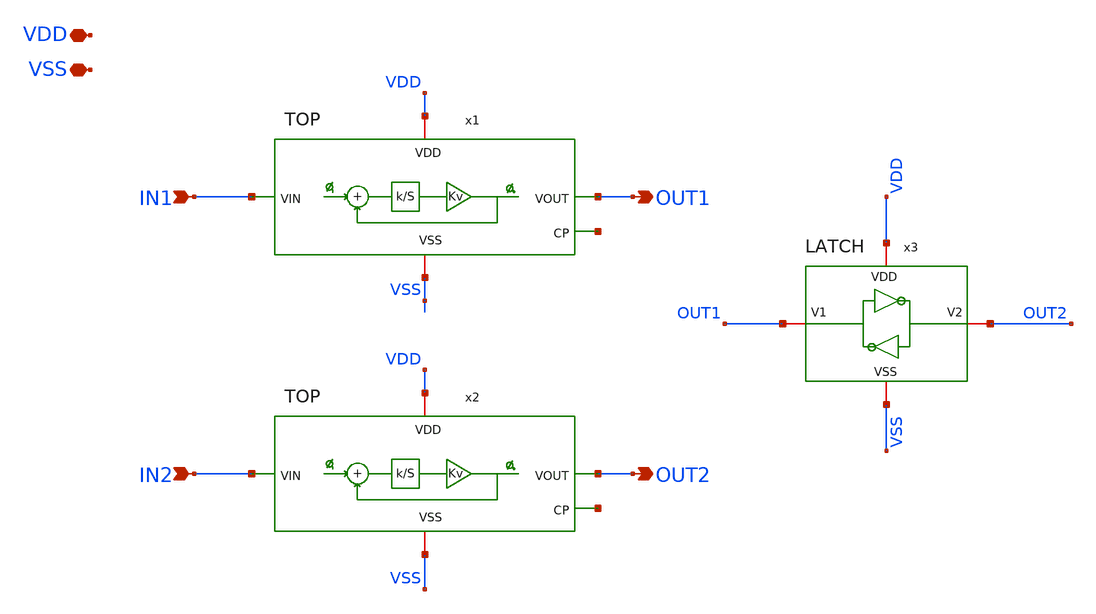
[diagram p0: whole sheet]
** sch_path: xschem/Cells/TOP_TOP.sch
**.subckt TOP_TOP VDD VSS IN1 IN2 OUT1 OUT2
*.iopin VDD
*.iopin VSS
*.ipin IN1
*.ipin IN2
*.opin OUT1
*.opin OUT2
x1 VDD OUT1 IN1 VSS net1 TOP
x2 VDD OUT2 IN2 VSS net2 TOP
x3 VSS OUT1 VDD OUT2 LATCH
**.ends
.end
